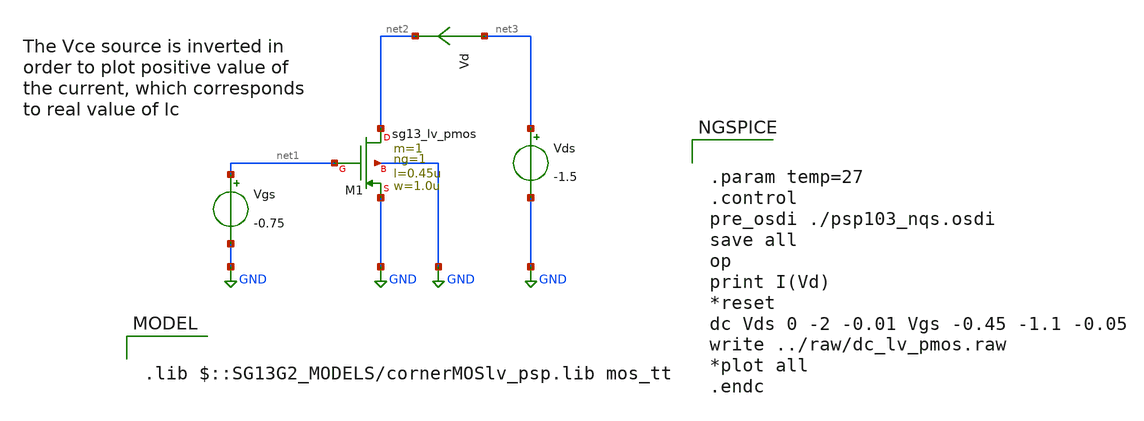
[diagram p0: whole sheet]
** sch_path: ihp-sg13g2/libs.tech/xschem/sg13g2_tests/dc_lv_pmos.sch
* Copyright 2023 IHP PDK Authors
**.subckt dc_lv_pmos
Vgs net1 GND -0.75
Vds net3 GND -1.5
XM1 net2 net1 GND GND sg13_lv_pmos w=1.0u l=0.45u ng=1 m=1 mm_ok=1
Vd net3 net2 0
.save i(vd)
**** begin user architecture code

.lib $::SG13G2_MODELS/cornerMOSlv_psp.lib mos_tt



.param temp=27
.control
pre_osdi ./psp103_nqs.osdi
save all
op
print I(Vd)
*reset
dc Vds 0 -2 -0.01 Vgs -0.45 -1.1 -0.05
write ../raw/dc_lv_pmos.raw
*plot all
.endc


**** end user architecture code
**.ends
.GLOBAL GND
.end
